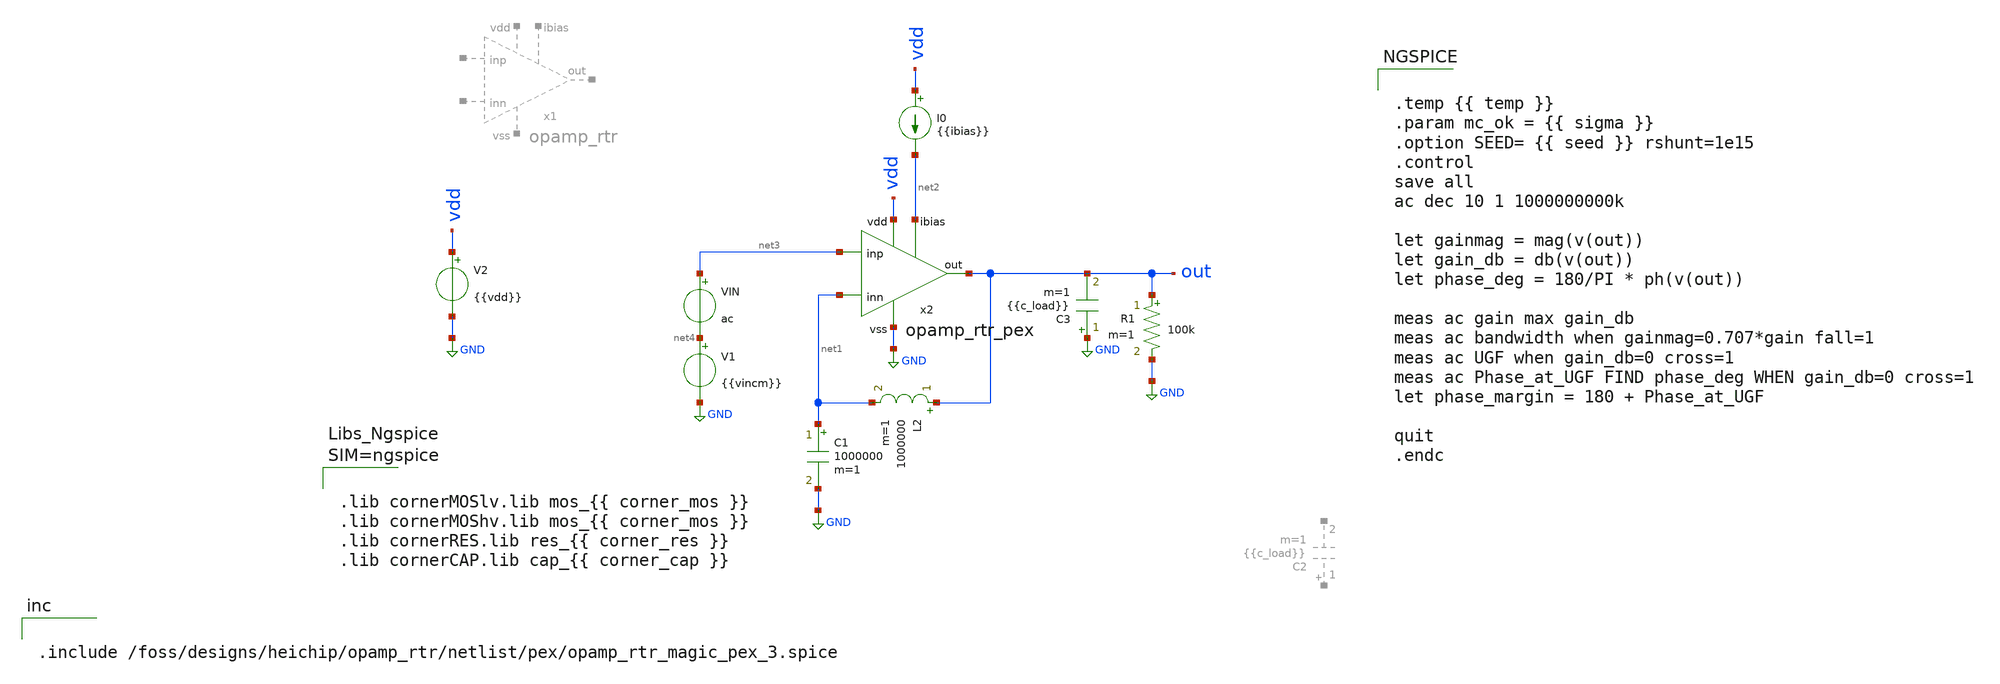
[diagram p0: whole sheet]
** sch_path: testbenches/xschem/tb_opamp_rtr_gain.sch
**.subckt tb_opamp_rtr_gain
V1 net4 GND {{vincm}}
.save i(v1)
V2 vdd GND {{vdd}}
VIN net3 net4 ac
.save i(vin)
L2 out net1 1000000 m=1
C1 net1 GND 1000000 m=1
I0 vdd net2 {{ibias}}
x2 vdd net3 GND net1 net2 out opamp_rtr_pex
C3 GND out {{c_load}} m=1
R1 out GND 100k m=1
**** begin user architecture code


.temp {{ temp }}
.param mc_ok = {{ sigma }}
.option SEED= {{ seed }} rshunt=1e15
.control
save all
ac dec 10 1 1000000000k

let gainmag = mag(v(out))
let gain_db = db(v(out))
let phase_deg = 180/PI * ph(v(out))

meas ac gain max gain_db
meas ac bandwidth when gainmag=0.707*gain fall=1
meas ac UGF when gain_db=0 cross=1
meas ac Phase_at_UGF FIND phase_deg WHEN gain_db=0 cross=1
let phase_margin = 180 + Phase_at_UGF

quit
.endc





.lib cornerMOSlv.lib mos_{{ corner_mos }}
.lib cornerMOShv.lib mos_{{ corner_mos }}
.lib cornerRES.lib res_{{ corner_res }}
.lib cornerCAP.lib cap_{{ corner_cap }}





.include /foss/designs/heichip/opamp_rtr/netlist/pex/opamp_rtr_magic_pex_3.spice


**** end user architecture code
**.ends

* expanding   symbol:  heichip/opamp_rtr/schematic/xschem/opamp_rtr.sym # of pins=6
** sym_path: schematic/xschem/opamp_rtr.sym
** sch_path: schematic/xschem/opamp_rtr.sch
.subckt opamp_rtr vdd inp vss inn ibias out
*.ipin inp
*.opin out
*.iopin vdd
*.ipin inn
*.ipin ibias
*.iopin vss
XXM6 out1_n inp ncmdiff_n net7 sg13_hv_nmos w={w_diff_n} l={l_diff} ng={n_diff_n} m=1 mm_ok=1
XXM1 net1 inn ncmdiff_p net8 sg13_hv_pmos w={w_diff_p} l={l_diff} ng={n_diff_p} m=1 mm_ok=1
XXM2 ncmdiff_p inp out1_p net9 sg13_hv_pmos w={w_diff_p} l={l_diff} ng={n_diff_p} m=1 mm_ok=1
XXM3 ncmdiff_p net10 vdd net11 sg13_hv_pmos w={w_tail_p} l={l_bias} ng={n_tail_p} m=1 mm_ok=1
XXM4 vss net1 net1 vss sg13_hv_nmos w={w_load_n} l={l_load} ng={n_load_n} m=1 mm_ok=1
XXM5 out1_p net1 vss vss sg13_hv_nmos w={w_load_n} l={l_load} ng={n_load_n} m=1 mm_ok=1
XXM7 ncmdiff_n inn net2 net12 sg13_hv_nmos w={w_diff_n} l={l_diff} ng={n_diff_n} m=1 mm_ok=1
XXM8 ncmdiff_n net13 vss net14 sg13_hv_nmos w={w_tail_n} l={l_bias} ng={n_tail_n} m=1 mm_ok=1
XXM9 vdd net2 out1_n net15 sg13_hv_pmos w={w_load_p} l={l_load} ng={n_load_p} m=1 mm_ok=1
XXM10 net2 net2 vdd net16 sg13_hv_pmos w={w_load_p} l={l_load} ng={n_load_p} m=1 mm_ok=1
XXM25 nswa vref_p ncmdiff_p ncmdiff_p sg13_hv_pmos w={w_sw_p} l={l_sw} ng={n_sw_p} m=1 mm_ok=1
XXM26 nswa nswa vss vss sg13_hv_nmos w={w_gmn} l={l_bias} ng={n_gmn} m=1 mm_ok=1
XXM27 ncmdiff_n nswa vss vss sg13_hv_nmos w={w_gmn} l={l_bias} ng={n_gmn} m=1 mm_ok=1
XXM28 ncmdiff_n vref_n nswb vss sg13_hv_nmos w={w_sw_n} l={l_sw} ng={n_sw_n} m=1 mm_ok=1
XXM29 nswb nswb vdd vdd sg13_hv_pmos w={w_gmp} l={l_bias} ng={n_gmp} m=1 mm_ok=1
XXM30 ncmdiff_p nswb vdd vdd sg13_hv_pmos w={w_gmp} l={l_bias} ng={n_gmp} m=1 mm_ok=1
XXM13 out1_n nabn out1_p vss sg13_hv_nmos w={w_ab_n} l={l_ab} ng={n_ab_n} m=1 mm_ok=1
XXM14 out1_p nabp out1_n vdd sg13_hv_pmos w={w_ab_p} l={l_ab} ng={n_ab_p} m=1 mm_ok=1
XXM15 out1_n vbias_p vdd vdd sg13_hv_pmos w={w_ab_src} l={l_bias} ng={n_ab_src} m=1 mm_ok=1
XXM16 out1_p nab_ref vss vss sg13_hv_nmos w={w_ab_snk} l={l_bias} ng={n_ab_snk} m=1 mm_ok=1
XXM23 nab_ref vbias_p vdd vdd sg13_hv_pmos w={w_ab_src} l={l_bias} ng={n_ab_src} m=1 mm_ok=1
XXM24 nab_ref nab_ref vss vss sg13_hv_nmos w={w_ab_snk} l={l_bias} ng={n_ab_snk} m=1 mm_ok=1
XXM17 nabn vbias_p vdd vdd sg13_hv_pmos w={w_ab_src} l={l_bias} ng={n_ab_src} m=1 mm_ok=1
XXM18 nabn nabn net3 vss sg13_hv_nmos w={w_ab_n} l={l_ab} ng={n_ab_n} m=1 mm_ok=1
XXM19 net3 net3 vss vss sg13_hv_nmos w={w_ab_n} l={l_ab} ng={n_ab_n} m=1 mm_ok=1
XXM20 nabp nab_ref vss vss sg13_hv_nmos w={w_ab_snk} l={l_bias} ng={n_ab_snk} m=1 mm_ok=1
XXM21 nabp nabp net4 vdd sg13_hv_pmos w={w_ab_p} l={l_ab} ng={n_ab_p} m=1 mm_ok=1
XXM22 net4 net4 vdd vdd sg13_hv_pmos w={w_ab_p} l={l_ab} ng={n_ab_p} m=1 mm_ok=1
XXM11 out out1_n vdd vdd sg13_hv_pmos w={w_out_p} l={l_out} ng={n_out_p} m=1 mm_ok=1
XXM12 out out1_p vss vss sg13_hv_nmos w={w_out_n} l={l_out} ng={n_out_n} m=1 mm_ok=1
R1 out net5 {r_null} m=1
C1 net5 out1_n {c_null} m=1
R2 out net6 {r_null} m=1
C2 net6 out1_p {c_null} m=1
XXB1 ibias ibias vss vss sg13_hv_nmos w={w_bias_n} l={l_bias} ng={n_bias_n} m=1 mm_ok=1
XXB2 vbias_p ibias vss vss sg13_hv_nmos w={w_bias_n} l={l_bias} ng={n_bias_n} m=1 mm_ok=1
XXB5 vref_n vref_n vss vss sg13_hv_nmos w={w_ref_n} l={l_bias} ng={n_ref_n} m=1 mm_ok=1
XXB6 vref_p ibias vss vss sg13_hv_nmos w={w_bias_n} l={l_bias} ng={n_bias_n} m=1 mm_ok=1
XXB3 vbias_p vbias_p vdd vdd sg13_hv_pmos w={w_bias_p} l={l_bias} ng={n_bias_p} m=1 mm_ok=1
XXB4 vref_n vbias_p vdd vdd sg13_hv_pmos w={w_bias_p} l={l_bias} ng={n_bias_p} m=1 mm_ok=1
XXB7 vref_p vref_p vdd vdd sg13_hv_pmos w={w_ref_p} l={l_bias} ng={n_ref_p} m=1 mm_ok=1
**** begin user architecture code



*bias network
.param l_bias=2u
.param w_bias_p=10u
.param w_bias_n=5u
.param w_ref_n=5u
.param w_ref_p=10u
*first stage
.param l_diff=1u
.param l_load=4u

.param w_diff_n=5u
.param n_diff_n=4

.param w_diff_p=10u
.param n_diff_p=4

.param w_load_n=5u
.param n_load_n=4

.param w_load_p=10u
.param n_load_p=4

.param w_tail_n=5u
.param n_tail_n=4

.param w_tail_p=10u
.param n_tail_p=4

.param l_sw=1u
.param w_sw_p=10u
.param n_sw_p=4

.param w_sw_n=5u
.param n_sw_n=4

.param w_gmn=5u
.param n_gmn=4

.param w_gmp=10u
.param n_gmp=4

*output control circuit
.param w_ab_src=10u
.param n_ab_src=4
.param w_ab_snk=5u
.param n_ab_snk=4

.param w_ab_n=5u
.param n_ab_n=4
.param w_ab_p=10u
.param n_ab_p=4

.param l_ab=1u

.param w_out_p=20u
.param n_out_p=4
.param w_out_n=10u
.param n_out_n=4

.param r_null=2k
.param c_null=200f




**** end user architecture code
.ends

.GLOBAL GND
.end
